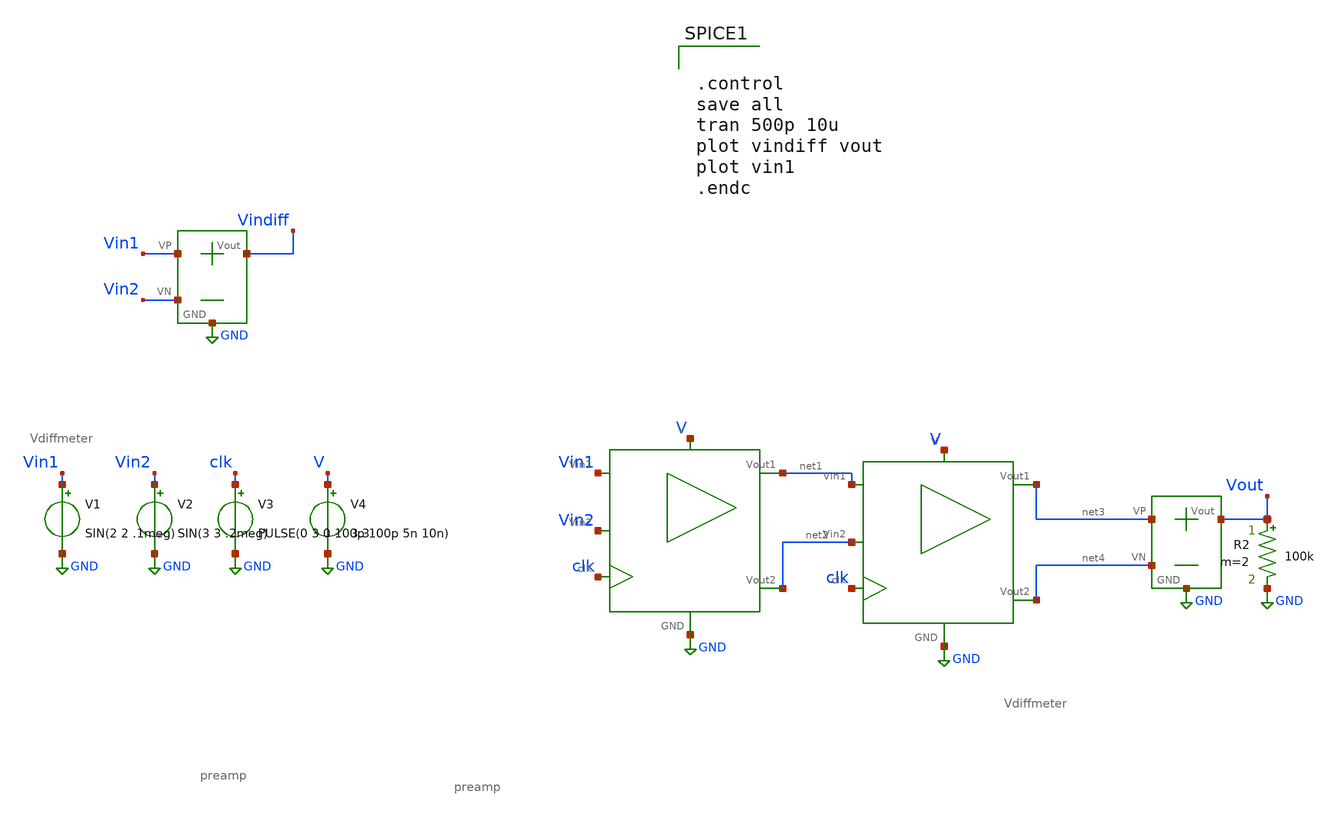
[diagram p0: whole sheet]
** sch_path: SAR_ADC/xschem/test/preamp_tb/cascada__tb.sch
**.subckt cascada__tb
V1 Vin1 GND SIN(2 2 .1meg)
V2 Vin2 GND SIN(3 3 .2meg)
V3 clk GND PULSE(0 3 0 100p 100p 5n 10n)
V4 V GND 3.3
X2 Vin1 Vin2 Vindiff GND Vdiffmeter
X1 V GND Vin1 clk net1 net2 Vin2 preamp
X3 net3 net4 Vout GND Vdiffmeter
R2 Vout GND 100k m=2
X4 V GND net1 clk net3 net4 net2 preamp
**** begin user architecture code


.control
save all
tran 500p 10u
plot vindiff vout
plot vin1
.endc


.include /foss/pdks/gf180mcuC/libs.tech/ngspice/design.ngspice
.lib /foss/pdks/gf180mcuC/libs.tech/ngspice/sm141064.ngspice typical

**** end user architecture code
**.ends
.GLOBAL GND
.end
